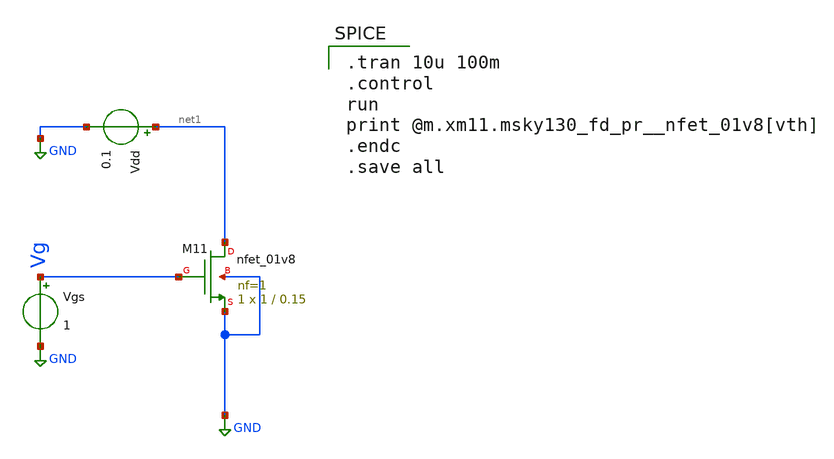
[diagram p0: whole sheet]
** sch_path: Blocks/Startup Converter/Vth_nmos.sch
**.subckt Vth_nmos
Vgs Vg GND 1
Vdd net1 GND 0.1
XM11 net1 Vg GND GND sky130_fd_pr__nfet_01v8 L=0.15 W=1 nf=1 ad='int((nf+1)/2) * W/nf * 0.29' as='int((nf+2)/2) * W/nf * 0.29'
+ pd='2*int((nf+1)/2) * (W/nf + 0.29)' ps='2*int((nf+2)/2) * (W/nf + 0.29)' nrd='0.29 / W' nrs='0.29 / W'
+ sa=0 sb=0 sd=0 mult=1 m=1
**** begin user architecture code

** opencircuitdesign pdks install
.lib $::SKYWATER_MODELS/sky130.lib.spice tt



.tran 10u 100m
.control
run
print @m.xm11.msky130_fd_pr__nfet_01v8[vth]
.endc
.save all

**** end user architecture code
**.ends
.GLOBAL GND
.end
